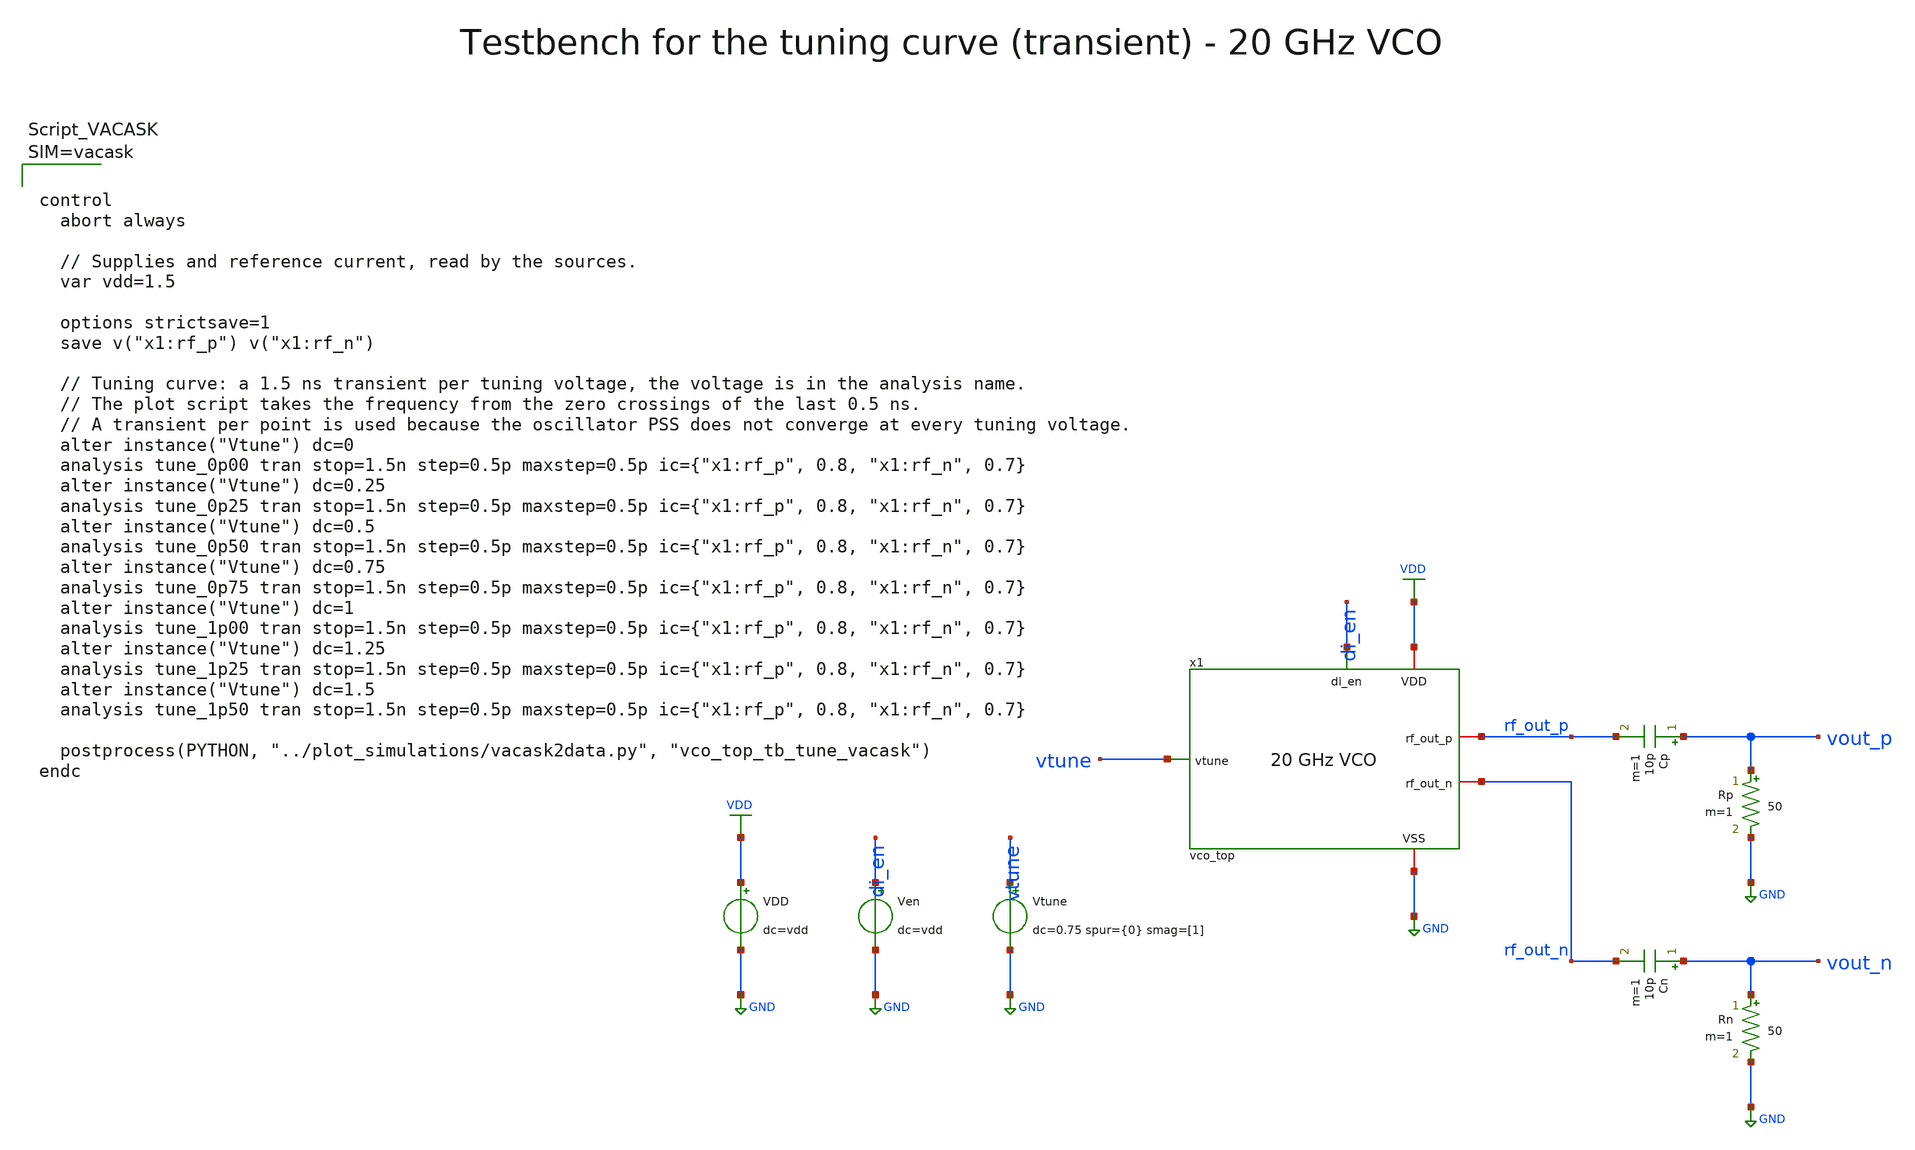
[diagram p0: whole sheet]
** sch_path: macros/vco/testbenches/xschem/vco_top_tb_tune_vacask.sch
**.subckt vco_top_tb_tune_vacask
x1 di_en VDD GND vtune rf_out_p rf_out_n vco_top
Cp vout_p rf_out_p 10p m=1
Rp vout_p GND 50 m=1
Cn vout_n rf_out_n 10p m=1
Rn vout_n GND 50 m=1
VDD VDD GND dc=vdd
Ven di_en GND dc=vdd
Vtune vtune GND dc=0.75 spur={0} smag=[1]
**** begin user architecture code






**** end user architecture code
**.ends

* expanding   symbol:  vco_top.sym # of pins=6
** sym_path: vco_top.sym
** sch_path: vco_top.sch
.subckt vco_top di_en VDD VSS vtune rf_out_p rf_out_n
*.iopin VDD
*.iopin VSS
*.ipin di_en
*.ipin vtune
*.iopin rf_out_p
*.iopin rf_out_n
xbias di_en VDD VSS vbg_buf vbn_buf en_b vco_bias
xcore vdd_core VSS vtune rf_p rf_n vco_core
xbuf vbn_buf vbg_buf VDD VSS rf_p rf_n rf_out_p rf_out_n vco_buf
xfeed en_b VDD VSS vdd_core vco_feed
xind rf_p rf_n vdd_core vco_ind_le
.ends


* expanding   symbol:  vco_bias.sym # of pins=6
** sym_path: vco_bias.sym
** sch_path: vco_bias.sch
.subckt vco_bias di_en VDD VSS vbg_buf vbn_buf en_b
*.iopin VDD
*.iopin VSS
*.ipin di_en
*.opin en_b
*.iopin vbn_buf
*.iopin vbg_buf
XMPi1 en_b di_en VDD VDD sg13_lv_pmos w=1u l=0.13u ng=1 m=1 mm_ok=1
XMNi1 en_b di_en VSS VSS sg13_lv_nmos w=0.5u l=0.13u ng=1 m=1 mm_ok=1
XMPi2 en en_b VDD VDD sg13_lv_pmos w=1u l=0.13u ng=1 m=1 mm_ok=1
XMNi2 en en_b VSS VSS sg13_lv_nmos w=0.5u l=0.13u ng=1 m=1 mm_ok=1
XMN0 ibias_100u ibias_100u VSS VSS sg13_lv_nmos w=2.5u l=0.5u ng=1 m=1 mm_ok=1
XMNd0 ibias_100u en_b VSS VSS sg13_lv_nmos w=1u l=0.13u ng=1 m=1 mm_ok=1
XRn ibias_100u vbn_buf VSS rhigh w=0.5e-6 l=32e-6 m=1 b=0 mm_ok=1
XMNd1 vbn_buf en_b VSS VSS sg13_lv_nmos w=1u l=0.13u ng=1 m=1 mm_ok=1
XMN1 vbp_ref ibias_100u VSS VSS sg13_lv_nmos w=2.5u l=0.5u ng=1 m=1 mm_ok=1
XMP1 vbp_ref vbp_ref VDD VDD sg13_lv_pmos w=5u l=0.5u ng=1 m=1 mm_ok=1
XMPd vbp_ref en VDD VDD sg13_lv_pmos w=1u l=0.13u ng=1 m=1 mm_ok=1
XMP2 vbg_int vbp_ref VDD VDD sg13_lv_pmos w=5u l=0.5u ng=1 m=1 mm_ok=1
XRg vbg_int nbg VSS rppd w=0.5e-6 l=8.5e-6 m=1 b=0 mm_ok=1
XMN3 nbg nbg VSS VSS sg13_lv_nmos w=2.5u l=0.5u ng=1 m=1 mm_ok=1
XMCn1 VSS vbn_buf VSS VSS sg13_lv_nmos w=40u l=10u ng=5 m=1 mm_ok=1
XMCn2 VSS vbn_buf VSS VSS sg13_lv_nmos w=40u l=10u ng=5 m=1 mm_ok=1
XRf vbg_int vbg_buf VSS rhigh w=0.5e-6 l=32e-6 m=1 b=0 mm_ok=1
XMCg1 VSS vbg_buf VSS VSS sg13_lv_nmos w=40u l=10u ng=5 m=1 mm_ok=1
XMCg2 VSS vbg_buf VSS VSS sg13_lv_nmos w=40u l=10u ng=5 m=1 mm_ok=1
XMDn1 VSS VSS VSS VSS sg13_lv_nmos w=2.5u l=0.5u ng=1 m=1 mm_ok=1
XMDn2 VSS VSS VSS VSS sg13_lv_nmos w=2.5u l=0.5u ng=1 m=1 mm_ok=1
XMDp1 VDD VDD VDD VDD sg13_lv_pmos w=5u l=0.5u ng=1 m=1 mm_ok=1
XMDp2 VDD VDD VDD VDD sg13_lv_pmos w=5u l=0.5u ng=1 m=1 mm_ok=1
XMPb nrb en_b VDD VDD sg13_lv_pmos w=2u l=0.13u ng=1 m=1 mm_ok=1
XMDp4 VDD VDD VDD VDD sg13_lv_pmos w=1u l=0.13u ng=1 m=1 mm_ok=1
XRb nrb ibias_100u VSS rppd w=0.5e-6 l=13.1e-6 m=1 b=0 mm_ok=1
XCg1 vbg_buf VSS cap_cmomf w=20.55e-6 l=18.7e-6 mmin=1 mmax=4 subblock=0 rfmodel=0 subscale=1 m=1
+ mm_ok=1
XCg2 vbg_buf VSS cap_cmomf w=8.58e-6 l=14.8e-6 mmin=1 mmax=4 subblock=0 rfmodel=0 subscale=1 m=1
+ mm_ok=1
.ends


* expanding   symbol:  vco_core.sym # of pins=5
** sym_path: vco_core.sym
** sch_path: vco_core.sch
.subckt vco_core vdd_core VSS vtune rf_p rf_n
*.iopin vdd_core
*.iopin VSS
*.ipin vtune
*.iopin rf_p
*.iopin rf_n
XCct1a1 vdd_core VSS cap_cmomf w=19e-6 l=26e-6 mmin=1 mmax=4 subblock=0 rfmodel=0 subscale=1 m=1
+ mm_ok=1
XCct1a2 vdd_core VSS cap_cmomf w=19e-6 l=26e-6 mmin=1 mmax=4 subblock=0 rfmodel=0 subscale=1 m=1
+ mm_ok=1
xvar rf_p rf_n vtune VSS vco_var
XM1 rf_p rf_n VSS VSS sg13_lv_nmos w=20u l=0.13u ng=10 m=1 mm_ok=1
XM2 rf_n rf_p VSS VSS sg13_lv_nmos w=20u l=0.13u ng=10 m=1 mm_ok=1
XCct2a vdd_core VSS cap_cmomf w=25.5e-6 l=19e-6 mmin=1 mmax=4 subblock=0 rfmodel=0 subscale=1 m=1
+ mm_ok=1
XCct1b1 VSS vdd_core cap_cmomf w=19e-6 l=26e-6 mmin=1 mmax=4 subblock=0 rfmodel=0 subscale=1 m=1
+ mm_ok=1
XCct1b2 VSS vdd_core cap_cmomf w=19e-6 l=26e-6 mmin=1 mmax=4 subblock=0 rfmodel=0 subscale=1 m=1
+ mm_ok=1
XCct2b VSS vdd_core cap_cmomf w=25.5e-6 l=19e-6 mmin=1 mmax=4 subblock=0 rfmodel=0 subscale=1 m=1
+ mm_ok=1
.ends


* expanding   symbol:  vco_buf.sym # of pins=8
** sym_path: vco_buf.sym
** sch_path: vco_buf.sch
.subckt vco_buf vbn_buf vbg_buf VDD VSS rf_p rf_n rf_out_p rf_out_n
*.iopin VDD
*.iopin VSS
*.iopin rf_out_n
*.iopin rf_out_p
*.ipin vbn_buf
*.iopin rf_p
*.iopin rf_n
*.ipin vbg_buf
XMB1 rf_out_n gp tail VSS sg13_lv_nmos w=24u l=0.13u ng=12 m=1 mm_ok=1
XMB2 rf_out_p gn tail VSS sg13_lv_nmos w=24u l=0.13u ng=12 m=1 mm_ok=1
XRL1 VDD rf_out_n VSS rppd w=10e-6 l=1.65e-6 m=1 b=0 mm_ok=1
XRL2 VDD rf_out_p VSS rppd w=10e-6 l=1.65e-6 m=1 b=0 mm_ok=1
XMBt tail vbn_buf VSS VSS sg13_lv_nmos w=150u l=0.5u ng=30 m=1 mm_ok=1
XCc1 gp rf_p cap_cmomf w=10e-6 l=18.6e-6 mmin=2 mmax=4 subblock=0 rfmodel=0 subscale=1 m=1 mm_ok=1
XCc2 gn rf_n cap_cmomf w=10e-6 l=18.6e-6 mmin=2 mmax=4 subblock=0 rfmodel=0 subscale=1 m=1 mm_ok=1
XRb1 vbg_buf gp VSS rhigh w=0.5e-6 l=8e-6 m=1 b=0 mm_ok=1
XRb2 vbg_buf gn VSS rhigh w=0.5e-6 l=8e-6 m=1 b=0 mm_ok=1
.ends


* expanding   symbol:  vco_feed.sym # of pins=4
** sym_path: vco_feed.sym
** sch_path: vco_feed.sch
.subckt vco_feed en_b VDD VSS vdd_core
*.iopin VDD
*.iopin VSS
*.ipin en_b
*.iopin vdd_core
XMPs n1 en_b VDD VDD sg13_lv_pmos w=96u l=0.13u ng=32 m=1 mm_ok=1
XRct n1 vdd_core VSS rppd w=17.3e-6 l=8.8e-6 m=1 b=0 mm_ok=1
.ends


* expanding   symbol:  vco_var.sym # of pins=4
** sym_path: vco_var.sym
** sch_path: vco_var.sch
.subckt vco_var rf_p rf_n vtune VSS
*.ipin vtune
*.iopin rf_p
*.iopin rf_n
*.iopin VSS
XCvar1 rf_p vtune rf_n VSS sg13_hv_svaricap w=3.74u l=0.3u Nx=8 mm_ok=1
XCvar2 rf_p vtune rf_n VSS sg13_hv_svaricap w=3.74u l=0.3u Nx=8 mm_ok=1
XCvar3 rf_p vtune rf_n VSS sg13_hv_svaricap w=3.74u l=0.3u Nx=8 mm_ok=1
.ends

.GLOBAL VDD
.GLOBAL GND
.end
